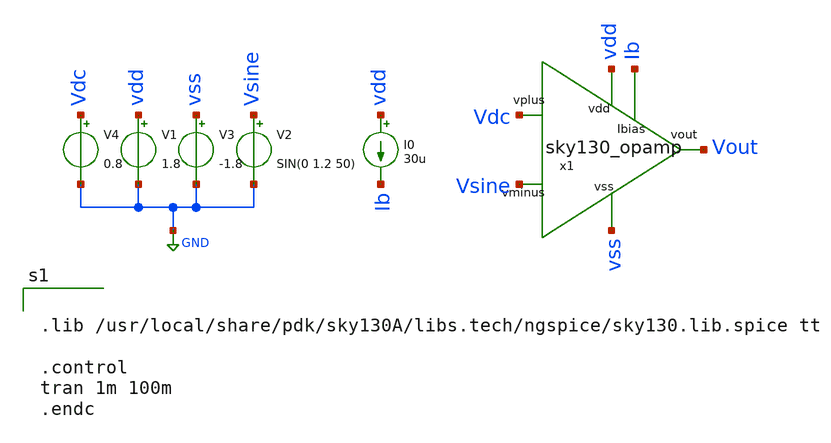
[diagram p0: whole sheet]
** sch_path: Primitives/Operational Amplifier/Xschem Files/opamp_test.sch
**.subckt opamp_test
x1 vdd Vout Vdc Vsine Ib vss sky130_opamp
V1 vdd GND 1.8
V2 Vsine GND SIN(0 1.2 50)
I0 vdd Ib 30u
V3 vss GND -1.8
V4 Vdc GND 0.8
**** begin user architecture code


.lib /usr/local/share/pdk/sky130A/libs.tech/ngspice/sky130.lib.spice tt

.control
tran 1m 100m
.endc


**** end user architecture code
**.ends

* expanding   symbol:  /home/rachtih/ADC trials/opamp/sky130_opamp.sym # of pins=6
** sym_path: Primitives/Operational Amplifier/Xschem Files/sky130_opamp.sym
** sch_path: Primitives/Operational Amplifier/Xschem Files/sky130_opamp.sch
.subckt sky130_opamp vdd vout vplus vminus Ibias vss
*.ipin Ibias
*.ipin vminus
*.ipin vplus
*.ipin vss
*.ipin vdd
*.opin vout
XM1 Ibias Ibias vss vss sky130_fd_pr__nfet_01v8 L=0.15 W=1 nf=1 ad='int((1 + 1)/2) * 1 / 1 * 0.29' as='int((1 + 2)/2) * 1 / 1 * 0.29'
+ pd='2*int((1 + 1)/2) * (1 / 1 + 0.29)' ps='2*int((1 + 2)/2) * (1 / 1 + 0.29)' nrd='0.29 / 1 ' nrs='0.29 / 1 '
+ sa=0 sb=0 sd=0 mult=1 m=1
XM2 net3 Ibias vss vss sky130_fd_pr__nfet_01v8 L=0.15 W=1 nf=1 ad='int((1 + 1)/2) * 1 / 1 * 0.29' as='int((1 + 2)/2) * 1 / 1 * 0.29'
+ pd='2*int((1 + 1)/2) * (1 / 1 + 0.29)' ps='2*int((1 + 2)/2) * (1 / 1 + 0.29)' nrd='0.29 / 1 ' nrs='0.29 / 1 '
+ sa=0 sb=0 sd=0 mult=1 m=1
XM3 net1 vminus net3 vss sky130_fd_pr__nfet_01v8 L=0.15 W=1 nf=1 ad='int((1 + 1)/2) * 1 / 1 * 0.29' as='int((1 + 2)/2) * 1 / 1 * 0.29'
+ pd='2*int((1 + 1)/2) * (1 / 1 + 0.29)' ps='2*int((1 + 2)/2) * (1 / 1 + 0.29)' nrd='0.29 / 1 ' nrs='0.29 / 1 '
+ sa=0 sb=0 sd=0 mult=1 m=1
XM4 net2 vplus net3 vss sky130_fd_pr__nfet_01v8 L=0.15 W=1 nf=1 ad='int((1 + 1)/2) * 1 / 1 * 0.29' as='int((1 + 2)/2) * 1 / 1 * 0.29'
+ pd='2*int((1 + 1)/2) * (1 / 1 + 0.29)' ps='2*int((1 + 2)/2) * (1 / 1 + 0.29)' nrd='0.29 / 1 ' nrs='0.29 / 1 '
+ sa=0 sb=0 sd=0 mult=1 m=1
XM5 vout Ibias vss vss sky130_fd_pr__nfet_01v8 L=0.15 W=1 nf=1 ad='int((1 + 1)/2) * 1 / 1 * 0.29' as='int((1 + 2)/2) * 1 / 1 * 0.29'
+ pd='2*int((1 + 1)/2) * (1 / 1 + 0.29)' ps='2*int((1 + 2)/2) * (1 / 1 + 0.29)' nrd='0.29 / 1 ' nrs='0.29 / 1 '
+ sa=0 sb=0 sd=0 mult=1 m=1
XM6 net2 net1 vdd vdd sky130_fd_pr__pfet_01v8 L=0.15 W=1 nf=1 ad='int((1 + 1)/2) * 1 / 1 * 0.29' as='int((1 + 2)/2) * 1 / 1 * 0.29'
+ pd='2*int((1 + 1)/2) * (1 / 1 + 0.29)' ps='2*int((1 + 2)/2) * (1 / 1 + 0.29)' nrd='0.29 / 1 ' nrs='0.29 / 1 '
+ sa=0 sb=0 sd=0 mult=1 m=1
XM7 net1 net1 vdd vdd sky130_fd_pr__pfet_01v8 L=0.15 W=1 nf=1 ad='int((1 + 1)/2) * 1 / 1 * 0.29' as='int((1 + 2)/2) * 1 / 1 * 0.29'
+ pd='2*int((1 + 1)/2) * (1 / 1 + 0.29)' ps='2*int((1 + 2)/2) * (1 / 1 + 0.29)' nrd='0.29 / 1 ' nrs='0.29 / 1 '
+ sa=0 sb=0 sd=0 mult=1 m=1
XM8 vout net2 vdd vdd sky130_fd_pr__pfet_01v8 L=0.15 W=1 nf=1 ad='int((1 + 1)/2) * 1 / 1 * 0.29' as='int((1 + 2)/2) * 1 / 1 * 0.29'
+ pd='2*int((1 + 1)/2) * (1 / 1 + 0.29)' ps='2*int((1 + 2)/2) * (1 / 1 + 0.29)' nrd='0.29 / 1 ' nrs='0.29 / 1 '
+ sa=0 sb=0 sd=0 mult=1 m=1
C1 net4 vout 2.7p m=1
R1 net2 net4 50 m=1
.ends

.GLOBAL GND
.end
